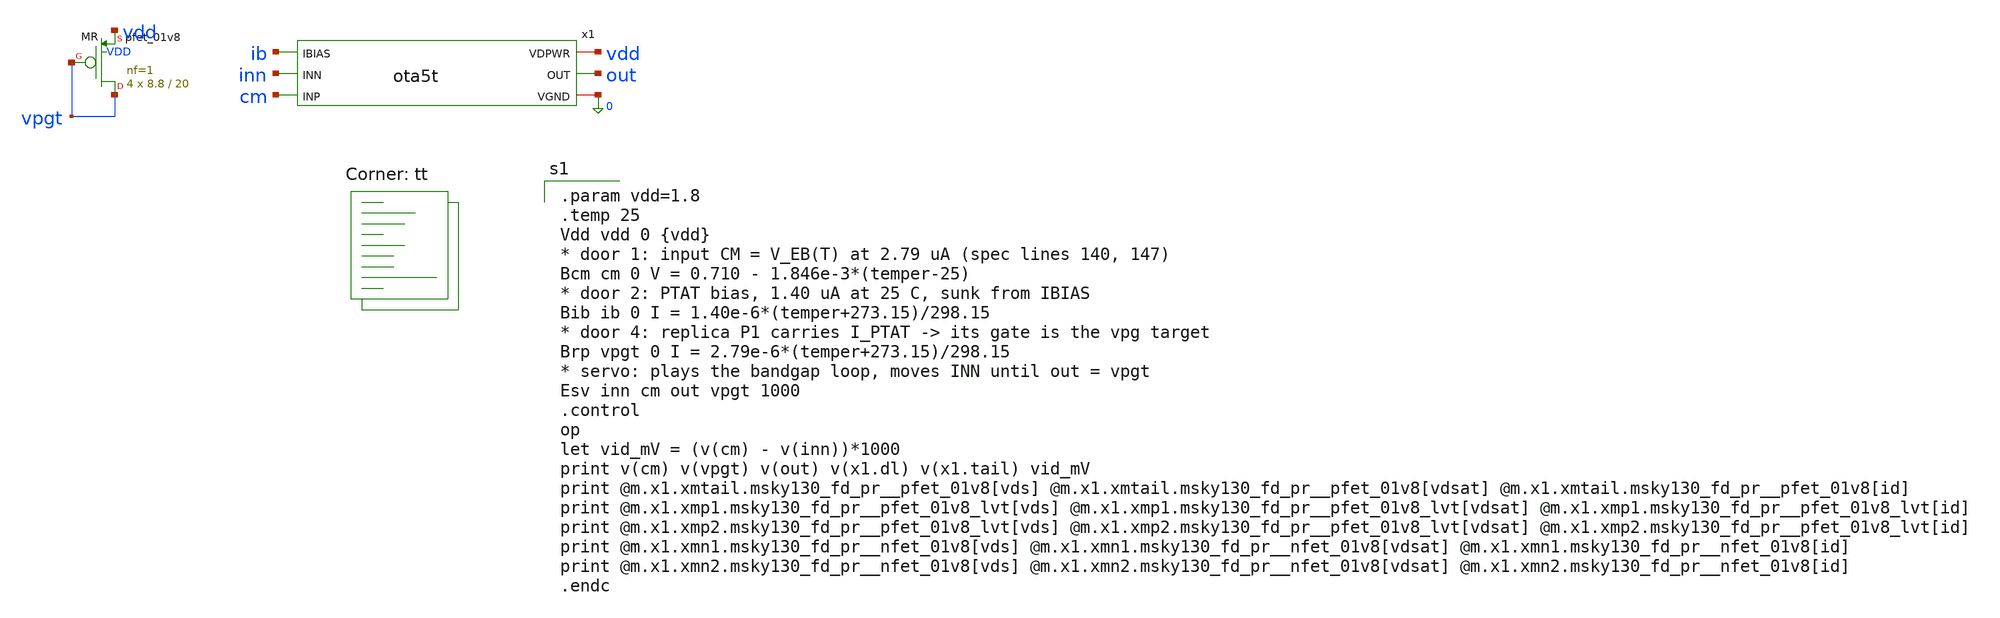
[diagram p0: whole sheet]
** sch_path: xschem/tb_ota5t_op.sch
**.subckt tb_ota5t_op
x1 vdd ib inn cm out 0 ota5t
XMR vpgt vpgt vdd VDD sky130_fd_pr__pfet_01v8 L=20 W=8.8 nf=1 ad='int((1 + 1)/2) * 8.8 / 1 * 0.29' as='int((1 + 2)/2) * 8.8 / 1 * 0.29'
+ pd='2*int((1 + 1)/2) * (8.8 / 1 + 0.29)' ps='2*int((1 + 2)/2) * (8.8 / 1 + 0.29)' nrd='0.29 / 8.8 ' nrs='0.29 / 8.8 '
+ sa=0 sb=0 sd=0 mult=4 m=4
**** begin user architecture code
.lib $::SKYWATER_MODELS/sky130.lib.spice tt

.param vdd=1.8
.temp 25
Vdd vdd 0 {vdd}
* door 1: input CM = V_EB(T) at 2.79 uA (spec lines 140, 147)
Bcm cm 0 V = 0.710 - 1.846e-3*(temper-25)
* door 2: PTAT bias, 1.40 uA at 25 C, sunk from IBIAS
Bib ib 0 I = 1.40e-6*(temper+273.15)/298.15
* door 4: replica P1 carries I_PTAT -> its gate is the vpg target
Brp vpgt 0 I = 2.79e-6*(temper+273.15)/298.15
* servo: plays the bandgap loop, moves INN until out = vpgt
Esv inn cm out vpgt 1000
.control
op
let vid_mV = (v(cm) - v(inn))*1000
print v(cm) v(vpgt) v(out) v(x1.dl) v(x1.tail) vid_mV
print @m.x1.xmtail.msky130_fd_pr__pfet_01v8[vds] @m.x1.xmtail.msky130_fd_pr__pfet_01v8[vdsat]
+ @m.x1.xmtail.msky130_fd_pr__pfet_01v8[id]
print @m.x1.xmp1.msky130_fd_pr__pfet_01v8_lvt[vds] @m.x1.xmp1.msky130_fd_pr__pfet_01v8_lvt[vdsat]
+ @m.x1.xmp1.msky130_fd_pr__pfet_01v8_lvt[id]
print @m.x1.xmp2.msky130_fd_pr__pfet_01v8_lvt[vds] @m.x1.xmp2.msky130_fd_pr__pfet_01v8_lvt[vdsat]
+ @m.x1.xmp2.msky130_fd_pr__pfet_01v8_lvt[id]
print @m.x1.xmn1.msky130_fd_pr__nfet_01v8[vds] @m.x1.xmn1.msky130_fd_pr__nfet_01v8[vdsat]
+ @m.x1.xmn1.msky130_fd_pr__nfet_01v8[id]
print @m.x1.xmn2.msky130_fd_pr__nfet_01v8[vds] @m.x1.xmn2.msky130_fd_pr__nfet_01v8[vdsat]
+ @m.x1.xmn2.msky130_fd_pr__nfet_01v8[id]
.endc

**** end user architecture code
**.ends

* expanding   symbol:  ota5t.sym # of pins=6
** sym_path: xschem/ota5t.sym
** sch_path: xschem/ota5t.sch
.subckt ota5t VDPWR IBIAS INN INP OUT VGND
*.ipin INP
*.ipin INN
*.ipin IBIAS
*.opin OUT
*.iopin VDPWR
*.iopin VGND
XMREF IBIAS IBIAS VDPWR VDPWR sky130_fd_pr__pfet_01v8 L=4 W=20 nf=1 ad='int((1 + 1)/2) * 20 / 1 * 0.29'
+ as='int((1 + 2)/2) * 20 / 1 * 0.29' pd='2*int((1 + 1)/2) * (20 / 1 + 0.29)' ps='2*int((1 + 2)/2) * (20 / 1 + 0.29)'
+ nrd='0.29 / 20 ' nrs='0.29 / 20 ' sa=0 sb=0 sd=0 mult=1 m=1
XMTAIL tail IBIAS VDPWR VDPWR sky130_fd_pr__pfet_01v8 L=4 W=20 nf=1 ad='int((1 + 1)/2) * 20 / 1 * 0.29'
+ as='int((1 + 2)/2) * 20 / 1 * 0.29' pd='2*int((1 + 1)/2) * (20 / 1 + 0.29)' ps='2*int((1 + 2)/2) * (20 / 1 + 0.29)'
+ nrd='0.29 / 20 ' nrs='0.29 / 20 ' sa=0 sb=0 sd=0 mult=2 m=2
XMP1 dl INP tail VDPWR sky130_fd_pr__pfet_01v8_lvt L=6 W=25 nf=1 ad='int((1 + 1)/2) * 25 / 1 * 0.29'
+ as='int((1 + 2)/2) * 25 / 1 * 0.29' pd='2*int((1 + 1)/2) * (25 / 1 + 0.29)' ps='2*int((1 + 2)/2) * (25 / 1 + 0.29)'
+ nrd='0.29 / 25 ' nrs='0.29 / 25 ' sa=0 sb=0 sd=0 mult=24 m=24
XMP2 OUT INN tail VDPWR sky130_fd_pr__pfet_01v8_lvt L=6 W=25 nf=1 ad='int((1 + 1)/2) * 25 / 1 * 0.29'
+ as='int((1 + 2)/2) * 25 / 1 * 0.29' pd='2*int((1 + 1)/2) * (25 / 1 + 0.29)' ps='2*int((1 + 2)/2) * (25 / 1 + 0.29)'
+ nrd='0.29 / 25 ' nrs='0.29 / 25 ' sa=0 sb=0 sd=0 mult=24 m=24
XMN1 dl dl VGND VGND sky130_fd_pr__nfet_01v8 L=20 W=6 nf=1 ad='int((1 + 1)/2) * 6 / 1 * 0.29' as='int((1 + 2)/2) * 6 / 1 * 0.29'
+ pd='2*int((1 + 1)/2) * (6 / 1 + 0.29)' ps='2*int((1 + 2)/2) * (6 / 1 + 0.29)' nrd='0.29 / 6 ' nrs='0.29 / 6 '
+ sa=0 sb=0 sd=0 mult=2 m=2
XMN2 OUT dl VGND VGND sky130_fd_pr__nfet_01v8 L=20 W=6 nf=1 ad='int((1 + 1)/2) * 6 / 1 * 0.29' as='int((1 + 2)/2) * 6 / 1 * 0.29'
+ pd='2*int((1 + 1)/2) * (6 / 1 + 0.29)' ps='2*int((1 + 2)/2) * (6 / 1 + 0.29)' nrd='0.29 / 6 ' nrs='0.29 / 6 '
+ sa=0 sb=0 sd=0 mult=2 m=2
.ends

.end
